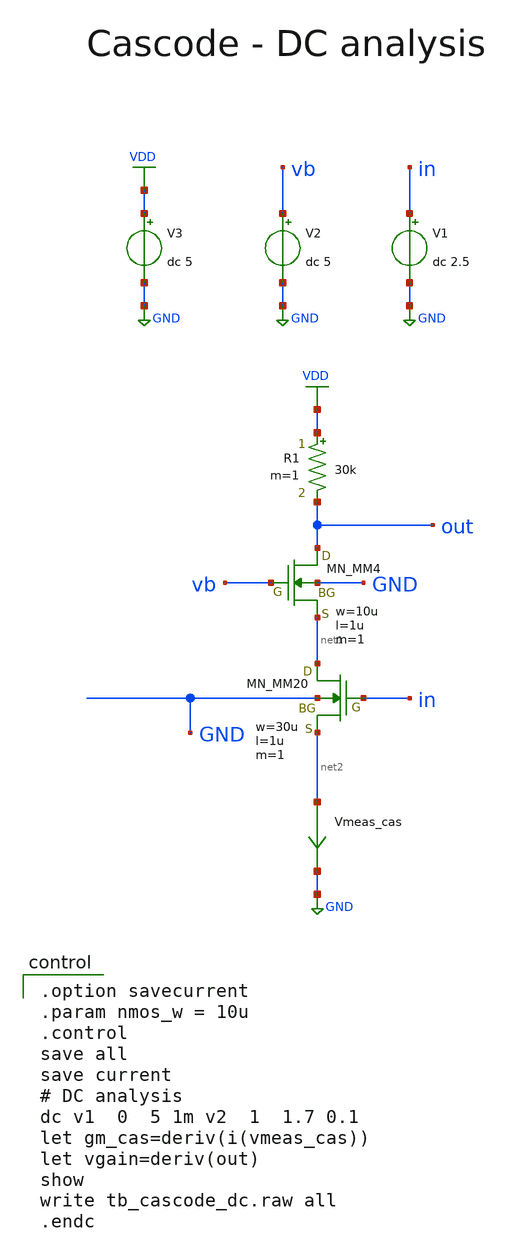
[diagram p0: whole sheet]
** sch_path: member_project/AM_Radio/Yamada3/xschem/tb_cascode.sch
**.subckt tb_cascode
V3 VDD GND dc 5
V1 in GND dc 2.5
MM4 out vb net1 GND NMOS w=10u l=1u as=0 ad=0 ps=0 pd=0 nrd=0 nrs=0 m=1
MM20 net1 in net2 GND NMOS w=30u l=1u as=0 ad=0 ps=0 pd=0 nrd=0 nrs=0 m=1
Vmeas_cas net2 GND 0
.save i(vmeas_cas)
R1 VDD out 30k m=1
V2 vb GND dc 5
**** begin user architecture code

.option savecurrent
.param nmos_w = 10u
.control
save all
save current
# DC analysis
dc v1  0  5 1m v2  1  1.7 0.1
let gm_cas=deriv(i(vmeas_cas))
let vgain=deriv(out)
show
write tb_cascode_dc.raw all
.endc

 .include $::LIB/ip62_models
**** end user architecture code
**.ends
.GLOBAL GND
.GLOBAL VDD
.end
